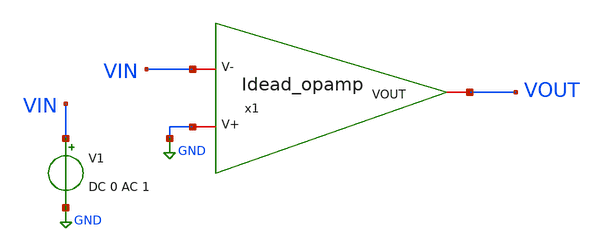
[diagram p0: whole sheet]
** sch_path: Design/Testbench_OL.sch
**.subckt Testbench_OL
x1 VOUT VIN GND Idead_opamp
V1 VIN GND DC 0 AC 1
**** begin user architecture code


ac


**** end user architecture code
**.ends

* expanding   symbol:  Idead_opamp.sym # of pins=3
** sym_path: Design/Idead_opamp.sym
** sch_path: Design/Idead_opamp.sch
.subckt Idead_opamp VOUT V- V+
*.iopin V-
*.iopin V+
*.iopin VOUT
E1 VOUT GND V+ V- 10000
.ends

.GLOBAL GND
.end
